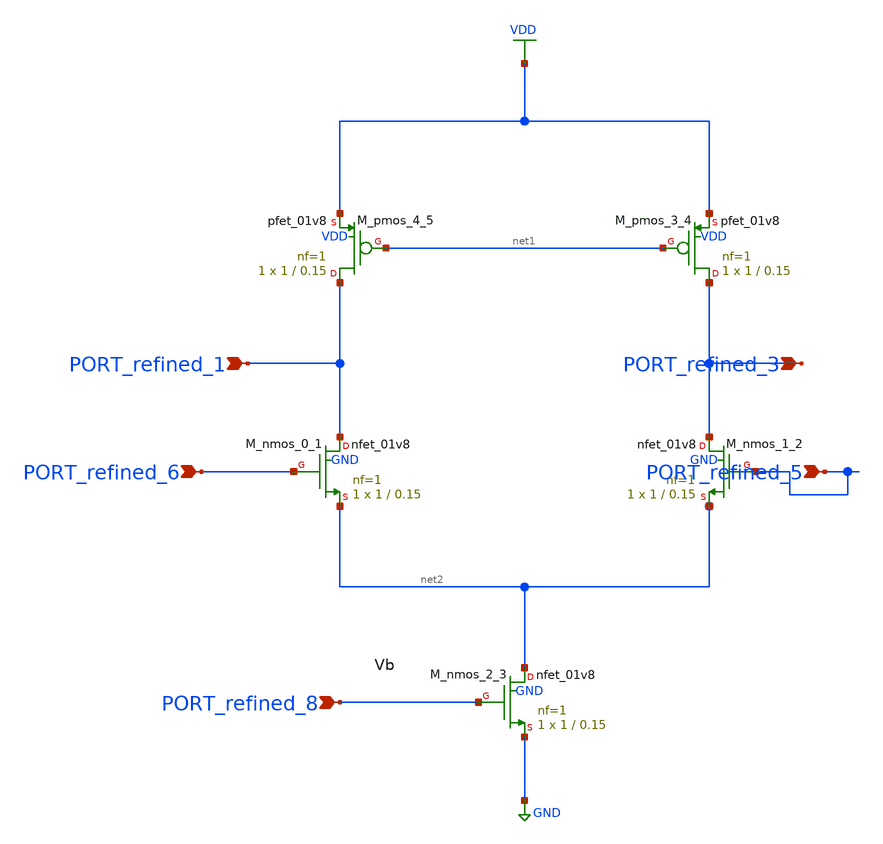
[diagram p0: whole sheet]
** sch_path: schematics/Image2Net/116.sch
**.subckt 116 PORT_refined_1 PORT_refined_8 PORT_refined_5 PORT_refined_6 PORT_refined_3
*.ipin PORT_refined_1
*.ipin PORT_refined_8
*.ipin PORT_refined_5
*.ipin PORT_refined_6
*.ipin PORT_refined_3
XM_nmos_0_1 PORT_refined_1 PORT_refined_6 net2 GND sky130_fd_pr__nfet_01v8 L=0.15 W=1 nf=1 ad='int((1 + 1)/2) * 1 / 1 * 0.29'
+ as='int((1 + 2)/2) * 1 / 1 * 0.29' pd='2*int((1 + 1)/2) * (1 / 1 + 0.29)' ps='2*int((1 + 2)/2) * (1 / 1 + 0.29)'
+ nrd='0.29 / 1 ' nrs='0.29 / 1 ' sa=0 sb=0 sd=0 mult=1 m=1
XM_nmos_1_2 PORT_refined_3 PORT_refined_5 net2 GND sky130_fd_pr__nfet_01v8 L=0.15 W=1 nf=1 ad='int((1 + 1)/2) * 1 / 1 * 0.29'
+ as='int((1 + 2)/2) * 1 / 1 * 0.29' pd='2*int((1 + 1)/2) * (1 / 1 + 0.29)' ps='2*int((1 + 2)/2) * (1 / 1 + 0.29)'
+ nrd='0.29 / 1 ' nrs='0.29 / 1 ' sa=0 sb=0 sd=0 mult=1 m=1
XM_nmos_2_3 net2 PORT_refined_8 GND GND sky130_fd_pr__nfet_01v8 L=0.15 W=1 nf=1 ad='int((1 + 1)/2) * 1 / 1 * 0.29'
+ as='int((1 + 2)/2) * 1 / 1 * 0.29' pd='2*int((1 + 1)/2) * (1 / 1 + 0.29)' ps='2*int((1 + 2)/2) * (1 / 1 + 0.29)'
+ nrd='0.29 / 1 ' nrs='0.29 / 1 ' sa=0 sb=0 sd=0 mult=1 m=1
XM_pmos_3_4 PORT_refined_3 net1 VDD VDD sky130_fd_pr__pfet_01v8 L=0.15 W=1 nf=1 ad='int((1 + 1)/2) * 1 / 1 * 0.29'
+ as='int((1 + 2)/2) * 1 / 1 * 0.29' pd='2*int((1 + 1)/2) * (1 / 1 + 0.29)' ps='2*int((1 + 2)/2) * (1 / 1 + 0.29)'
+ nrd='0.29 / 1 ' nrs='0.29 / 1 ' sa=0 sb=0 sd=0 mult=1 m=1
XM_pmos_4_5 PORT_refined_1 net1 VDD VDD sky130_fd_pr__pfet_01v8 L=0.15 W=1 nf=1 ad='int((1 + 1)/2) * 1 / 1 * 0.29'
+ as='int((1 + 2)/2) * 1 / 1 * 0.29' pd='2*int((1 + 1)/2) * (1 / 1 + 0.29)' ps='2*int((1 + 2)/2) * (1 / 1 + 0.29)'
+ nrd='0.29 / 1 ' nrs='0.29 / 1 ' sa=0 sb=0 sd=0 mult=1 m=1
**.ends
.GLOBAL GND
.GLOBAL VDD
.end
